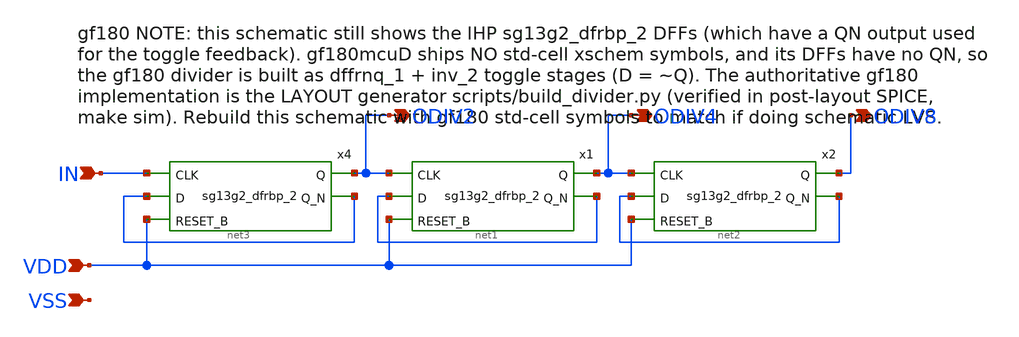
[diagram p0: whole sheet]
** sch_path: xschem/freq_divider.sch
**.subckt freq_divider IN ODIV2 ODIV4 ODIV8 VDD VSS
*.ipin IN
*.opin ODIV2
*.opin ODIV4
*.opin ODIV8
*.ipin VDD
*.ipin VSS
x4 ODIV2 net3 IN net3 VDD VDD VSS sg13g2_dfrbp_2
x1 ODIV4 net1 ODIV2 net1 VDD VDD VSS sg13g2_dfrbp_2
x2 ODIV8 net2 ODIV4 net2 VDD VDD VSS sg13g2_dfrbp_2
**.ends

* expanding   symbol:  sg13g2_stdcells/sg13g2_dfrbp_2.sym # of pins=5
** sym_path: sg13g2_stdcells/sg13g2_dfrbp_2.sym
** sch_path: sg13g2_stdcells/sg13g2_dfrbp_2.sch
.subckt sg13g2_dfrbp_2 Q Q_N CLK D RESET_B VDD VSS
*.ipin D
*.ipin RESET_B
*.ipin CLK
*.opin Q
*.opin Q_N
*.iopin VDD
*.iopin VSS
XM1 Db D net12 VSS sg13_lv_nmos w=420.00n l=130.00n ng=1 m=1 mm_ok=1
XM2 net12 RESET_B VSS VSS sg13_lv_nmos w=420.00n l=130.00n ng=1 m=1 mm_ok=1
XM3 net2 clkneg net11 VSS sg13_lv_nmos w=420.00n l=130.00n ng=1 m=1 mm_ok=1
XM4 net11 net3 VSS VSS sg13_lv_nmos w=420.00n l=130.00n ng=1 m=1 mm_ok=1
XM5 net3 net2 net7 VSS sg13_lv_nmos w=420.00n l=130.00n ng=1 m=1 mm_ok=1
XM6 net7 RESET_B VSS VSS sg13_lv_nmos w=420.00n l=130.00n ng=1 m=1 mm_ok=1
XM7 Q_N net2 VSS VSS sg13_lv_nmos w=1.48u l=130.00n ng=2 m=1 mm_ok=1
XM8 net1 net2 VSS VSS sg13_lv_nmos w=640.00n l=130.00n ng=1 m=1 mm_ok=1
XM9 Q net1 VSS VSS sg13_lv_nmos w=1.48u l=130.00n ng=2 m=1 mm_ok=1
XM10 clkneg CLK VSS VSS sg13_lv_nmos w=740.00n l=130.00n ng=1 m=1 mm_ok=1
XM11 clkpos clkneg VSS VSS sg13_lv_nmos w=740.00n l=130.00n ng=1 m=1 mm_ok=1
XM12 Db clkneg net4 VSS sg13_lv_nmos w=420.00n l=130.00n ng=1 m=1 mm_ok=1
XM13 net4 clkpos net10 VSS sg13_lv_nmos w=420.00n l=130.00n ng=1 m=1 mm_ok=1
XM14 net10 net5 net6 VSS sg13_lv_nmos w=420.00n l=130.00n ng=1 m=1 mm_ok=1
XM15 net6 RESET_B VSS VSS sg13_lv_nmos w=420.00n l=130.00n ng=1 m=1 mm_ok=1
XM16 net5 net4 VSS VSS sg13_lv_nmos w=740.00n l=130.00n ng=1 m=1 mm_ok=1
XM17 net5 clkpos net2 VSS sg13_lv_nmos w=740.00n l=130.00n ng=1 m=1 mm_ok=1
XM18 Db RESET_B VDD VDD sg13_lv_pmos w=420.00n l=130.00n ng=1 m=1 mm_ok=1
XM19 Db D VDD VDD sg13_lv_pmos w=420.00n l=130.00n ng=1 m=1 mm_ok=1
XM20 net9 net3 VDD VDD sg13_lv_pmos w=420.00n l=130.00n ng=1 m=1 mm_ok=1
XM21 net2 clkpos net9 VDD sg13_lv_pmos w=420.00n l=130.00n ng=1 m=1 mm_ok=1
XM22 net3 net2 VDD VDD sg13_lv_pmos w=420.00n l=130.00n ng=1 m=1 mm_ok=1
XM23 net3 RESET_B VDD VDD sg13_lv_pmos w=420.00n l=130.00n ng=1 m=1 mm_ok=1
XM24 Q_N net2 VDD VDD sg13_lv_pmos w=2.24u l=130.00n ng=2 m=1 mm_ok=1
XM25 net1 net2 VDD VDD sg13_lv_pmos w=1.000u l=130.00n ng=1 m=1 mm_ok=1
XM26 Q net1 VDD VDD sg13_lv_pmos w=2.24u l=130.00n ng=2 m=1 mm_ok=1
XM27 clkneg CLK VDD VDD sg13_lv_pmos w=1.12u l=130.00n ng=1 m=1 mm_ok=1
XM28 clkpos clkneg VDD VDD sg13_lv_pmos w=1.12u l=130.00n ng=1 m=1 mm_ok=1
XM29 Db clkpos net4 VDD sg13_lv_pmos w=420.00n l=130.00n ng=1 m=1 mm_ok=1
XM30 net8 net5 VDD VDD sg13_lv_pmos w=420.00n l=130.00n ng=1 m=1 mm_ok=1
XM31 net4 clkneg net8 VDD sg13_lv_pmos w=420.00n l=130.00n ng=1 m=1 mm_ok=1
XM32 net4 RESET_B VDD VDD sg13_lv_pmos w=420.00n l=130.00n ng=1 m=1 mm_ok=1
XM33 net5 net4 VDD VDD sg13_lv_pmos w=1.000u l=130.00n ng=1 m=1 mm_ok=1
XM34 net5 clkneg net2 VDD sg13_lv_pmos w=1.000u l=130.00n ng=1 m=1 mm_ok=1
.ends

.end
